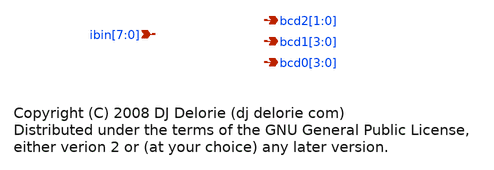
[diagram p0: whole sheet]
** sch_path: xschem_libs_newsym/binto7seg/bcd/schematic/bcd.sch
* Copyright (C) 1998-2024 Stefan Frederik Schippers
* This program is free software; you can redistribute it and/or modify
* it under the terms of the GNU General Public License as published by
* the Free Software Foundation; either version 2 of the License, or
* (at your option) any later version.
* This program is distributed in the hope that it will be useful,
* but WITHOUT ANY WARRANTY; without even the implied warranty of
* MERCHANTABILITY or FITNESS FOR A PARTICULAR PURPOSE.  See the
* GNU General Public License for more details.
* You should have received a copy of the GNU General Public License
* along with this program; if not, write to the Free Software
* C {devices/code} 260 -380 0 0 {name=CODE value="// Copyright (C) 2008 DJ Delorie <dj delorie com>
**.subckt bcd ibin[7],ibin[6],ibin[5],ibin[4],ibin[3],ibin[2],ibin[1],ibin[0] bcd2[1],bcd2[0]
*+ bcd1[3],bcd1[2],bcd1[1],bcd1[0] bcd0[3],bcd0[2],bcd0[1],bcd0[0]
*.ipin ibin[7],ibin[6],ibin[5],ibin[4],ibin[3],ibin[2],ibin[1],ibin[0]
*.opin bcd2[1],bcd2[0]
*.opin bcd1[3],bcd1[2],bcd1[1],bcd1[0]
*.opin bcd0[3],bcd0[2],bcd0[1],bcd0[0]
**** begin user architecture code

// Copyright (C) 2008 DJ Delorie <dj delorie com>
// Distributed under the terms of the GNU General Public License,
// either verion 2 or (at your choice) any later version.

always @ (ibin)
begin

  case (ibin)
    0 : begin bcd2 <= 2'b00; bcd1 <= 4'b0000; bcd0 <= 4'b0000; end
    1 : begin bcd2 <= 2'b00; bcd1 <= 4'b0000; bcd0 <= 4'b0001; end
    2 : begin bcd2 <= 2'b00; bcd1 <= 4'b0000; bcd0 <= 4'b0010; end
    3 : begin bcd2 <= 2'b00; bcd1 <= 4'b0000; bcd0 <= 4'b0011; end
    4 : begin bcd2 <= 2'b00; bcd1 <= 4'b0000; bcd0 <= 4'b0100; end
    5 : begin bcd2 <= 2'b00; bcd1 <= 4'b0000; bcd0 <= 4'b0101; end
    6 : begin bcd2 <= 2'b00; bcd1 <= 4'b0000; bcd0 <= 4'b0110; end
    7 : begin bcd2 <= 2'b00; bcd1 <= 4'b0000; bcd0 <= 4'b0111; end
    8 : begin bcd2 <= 2'b00; bcd1 <= 4'b0000; bcd0 <= 4'b1000; end
    9 : begin bcd2 <= 2'b00; bcd1 <= 4'b0000; bcd0 <= 4'b1001; end
    10 : begin bcd2 <= 2'b00; bcd1 <= 4'b0001; bcd0 <= 4'b0000; end
    11 : begin bcd2 <= 2'b00; bcd1 <= 4'b0001; bcd0 <= 4'b0001; end
    12 : begin bcd2 <= 2'b00; bcd1 <= 4'b0001; bcd0 <= 4'b0010; end
    13 : begin bcd2 <= 2'b00; bcd1 <= 4'b0001; bcd0 <= 4'b0011; end
    14 : begin bcd2 <= 2'b00; bcd1 <= 4'b0001; bcd0 <= 4'b0100; end
    15 : begin bcd2 <= 2'b00; bcd1 <= 4'b0001; bcd0 <= 4'b0101; end
    16 : begin bcd2 <= 2'b00; bcd1 <= 4'b0001; bcd0 <= 4'b0110; end
    17 : begin bcd2 <= 2'b00; bcd1 <= 4'b0001; bcd0 <= 4'b0111; end
    18 : begin bcd2 <= 2'b00; bcd1 <= 4'b0001; bcd0 <= 4'b1000; end
    19 : begin bcd2 <= 2'b00; bcd1 <= 4'b0001; bcd0 <= 4'b1001; end
    20 : begin bcd2 <= 2'b00; bcd1 <= 4'b0010; bcd0 <= 4'b0000; end
    21 : begin bcd2 <= 2'b00; bcd1 <= 4'b0010; bcd0 <= 4'b0001; end
    22 : begin bcd2 <= 2'b00; bcd1 <= 4'b0010; bcd0 <= 4'b0010; end
    23 : begin bcd2 <= 2'b00; bcd1 <= 4'b0010; bcd0 <= 4'b0011; end
    24 : begin bcd2 <= 2'b00; bcd1 <= 4'b0010; bcd0 <= 4'b0100; end
    25 : begin bcd2 <= 2'b00; bcd1 <= 4'b0010; bcd0 <= 4'b0101; end
    26 : begin bcd2 <= 2'b00; bcd1 <= 4'b0010; bcd0 <= 4'b0110; end
    27 : begin bcd2 <= 2'b00; bcd1 <= 4'b0010; bcd0 <= 4'b0111; end
    28 : begin bcd2 <= 2'b00; bcd1 <= 4'b0010; bcd0 <= 4'b1000; end
    29 : begin bcd2 <= 2'b00; bcd1 <= 4'b0010; bcd0 <= 4'b1001; end
    30 : begin bcd2 <= 2'b00; bcd1 <= 4'b0011; bcd0 <= 4'b0000; end
    31 : begin bcd2 <= 2'b00; bcd1 <= 4'b0011; bcd0 <= 4'b0001; end
    32 : begin bcd2 <= 2'b00; bcd1 <= 4'b0011; bcd0 <= 4'b0010; end
    33 : begin bcd2 <= 2'b00; bcd1 <= 4'b0011; bcd0 <= 4'b0011; end
    34 : begin bcd2 <= 2'b00; bcd1 <= 4'b0011; bcd0 <= 4'b0100; end
    35 : begin bcd2 <= 2'b00; bcd1 <= 4'b0011; bcd0 <= 4'b0101; end
    36 : begin bcd2 <= 2'b00; bcd1 <= 4'b0011; bcd0 <= 4'b0110; end
    37 : begin bcd2 <= 2'b00; bcd1 <= 4'b0011; bcd0 <= 4'b0111; end
    38 : begin bcd2 <= 2'b00; bcd1 <= 4'b0011; bcd0 <= 4'b1000; end
    39 : begin bcd2 <= 2'b00; bcd1 <= 4'b0011; bcd0 <= 4'b1001; end
    40 : begin bcd2 <= 2'b00; bcd1 <= 4'b0100; bcd0 <= 4'b0000; end
    41 : begin bcd2 <= 2'b00; bcd1 <= 4'b0100; bcd0 <= 4'b0001; end
    42 : begin bcd2 <= 2'b00; bcd1 <= 4'b0100; bcd0 <= 4'b0010; end
    43 : begin bcd2 <= 2'b00; bcd1 <= 4'b0100; bcd0 <= 4'b0011; end
    44 : begin bcd2 <= 2'b00; bcd1 <= 4'b0100; bcd0 <= 4'b0100; end
    45 : begin bcd2 <= 2'b00; bcd1 <= 4'b0100; bcd0 <= 4'b0101; end
    46 : begin bcd2 <= 2'b00; bcd1 <= 4'b0100; bcd0 <= 4'b0110; end
    47 : begin bcd2 <= 2'b00; bcd1 <= 4'b0100; bcd0 <= 4'b0111; end
    48 : begin bcd2 <= 2'b00; bcd1 <= 4'b0100; bcd0 <= 4'b1000; end
    49 : begin bcd2 <= 2'b00; bcd1 <= 4'b0100; bcd0 <= 4'b1001; end
    50 : begin bcd2 <= 2'b00; bcd1 <= 4'b0101; bcd0 <= 4'b0000; end
    51 : begin bcd2 <= 2'b00; bcd1 <= 4'b0101; bcd0 <= 4'b0001; end
    52 : begin bcd2 <= 2'b00; bcd1 <= 4'b0101; bcd0 <= 4'b0010; end
    53 : begin bcd2 <= 2'b00; bcd1 <= 4'b0101; bcd0 <= 4'b0011; end
    54 : begin bcd2 <= 2'b00; bcd1 <= 4'b0101; bcd0 <= 4'b0100; end
    55 : begin bcd2 <= 2'b00; bcd1 <= 4'b0101; bcd0 <= 4'b0101; end
    56 : begin bcd2 <= 2'b00; bcd1 <= 4'b0101; bcd0 <= 4'b0110; end
    57 : begin bcd2 <= 2'b00; bcd1 <= 4'b0101; bcd0 <= 4'b0111; end
    58 : begin bcd2 <= 2'b00; bcd1 <= 4'b0101; bcd0 <= 4'b1000; end
    59 : begin bcd2 <= 2'b00; bcd1 <= 4'b0101; bcd0 <= 4'b1001; end
    60 : begin bcd2 <= 2'b00; bcd1 <= 4'b0110; bcd0 <= 4'b0000; end
    61 : begin bcd2 <= 2'b00; bcd1 <= 4'b0110; bcd0 <= 4'b0001; end
    62 : begin bcd2 <= 2'b00; bcd1 <= 4'b0110; bcd0 <= 4'b0010; end
    63 : begin bcd2 <= 2'b00; bcd1 <= 4'b0110; bcd0 <= 4'b0011; end
    64 : begin bcd2 <= 2'b00; bcd1 <= 4'b0110; bcd0 <= 4'b0100; end
    65 : begin bcd2 <= 2'b00; bcd1 <= 4'b0110; bcd0 <= 4'b0101; end
    66 : begin bcd2 <= 2'b00; bcd1 <= 4'b0110; bcd0 <= 4'b0110; end
    67 : begin bcd2 <= 2'b00; bcd1 <= 4'b0110; bcd0 <= 4'b0111; end
    68 : begin bcd2 <= 2'b00; bcd1 <= 4'b0110; bcd0 <= 4'b1000; end
    69 : begin bcd2 <= 2'b00; bcd1 <= 4'b0110; bcd0 <= 4'b1001; end
    70 : begin bcd2 <= 2'b00; bcd1 <= 4'b0111; bcd0 <= 4'b0000; end
    71 : begin bcd2 <= 2'b00; bcd1 <= 4'b0111; bcd0 <= 4'b0001; end
    72 : begin bcd2 <= 2'b00; bcd1 <= 4'b0111; bcd0 <= 4'b0010; end
    73 : begin bcd2 <= 2'b00; bcd1 <= 4'b0111; bcd0 <= 4'b0011; end
    74 : begin bcd2 <= 2'b00; bcd1 <= 4'b0111; bcd0 <= 4'b0100; end
    75 : begin bcd2 <= 2'b00; bcd1 <= 4'b0111; bcd0 <= 4'b0101; end
    76 : begin bcd2 <= 2'b00; bcd1 <= 4'b0111; bcd0 <= 4'b0110; end
    77 : begin bcd2 <= 2'b00; bcd1 <= 4'b0111; bcd0 <= 4'b0111; end
    78 : begin bcd2 <= 2'b00; bcd1 <= 4'b0111; bcd0 <= 4'b1000; end
    79 : begin bcd2 <= 2'b00; bcd1 <= 4'b0111; bcd0 <= 4'b1001; end
    80 : begin bcd2 <= 2'b00; bcd1 <= 4'b1000; bcd0 <= 4'b0000; end
    81 : begin bcd2 <= 2'b00; bcd1 <= 4'b1000; bcd0 <= 4'b0001; end
    82 : begin bcd2 <= 2'b00; bcd1 <= 4'b1000; bcd0 <= 4'b0010; end
    83 : begin bcd2 <= 2'b00; bcd1 <= 4'b1000; bcd0 <= 4'b0011; end
    84 : begin bcd2 <= 2'b00; bcd1 <= 4'b1000; bcd0 <= 4'b0100; end
    85 : begin bcd2 <= 2'b00; bcd1 <= 4'b1000; bcd0 <= 4'b0101; end
    86 : begin bcd2 <= 2'b00; bcd1 <= 4'b1000; bcd0 <= 4'b0110; end
    87 : begin bcd2 <= 2'b00; bcd1 <= 4'b1000; bcd0 <= 4'b0111; end
    88 : begin bcd2 <= 2'b00; bcd1 <= 4'b1000; bcd0 <= 4'b1000; end
    89 : begin bcd2 <= 2'b00; bcd1 <= 4'b1000; bcd0 <= 4'b1001; end
    90 : begin bcd2 <= 2'b00; bcd1 <= 4'b1001; bcd0 <= 4'b0000; end
    91 : begin bcd2 <= 2'b00; bcd1 <= 4'b1001; bcd0 <= 4'b0001; end
    92 : begin bcd2 <= 2'b00; bcd1 <= 4'b1001; bcd0 <= 4'b0010; end
    93 : begin bcd2 <= 2'b00; bcd1 <= 4'b1001; bcd0 <= 4'b0011; end
    94 : begin bcd2 <= 2'b00; bcd1 <= 4'b1001; bcd0 <= 4'b0100; end
    95 : begin bcd2 <= 2'b00; bcd1 <= 4'b1001; bcd0 <= 4'b0101; end
    96 : begin bcd2 <= 2'b00; bcd1 <= 4'b1001; bcd0 <= 4'b0110; end
    97 : begin bcd2 <= 2'b00; bcd1 <= 4'b1001; bcd0 <= 4'b0111; end
    98 : begin bcd2 <= 2'b00; bcd1 <= 4'b1001; bcd0 <= 4'b1000; end
    99 : begin bcd2 <= 2'b00; bcd1 <= 4'b1001; bcd0 <= 4'b1001; end
    100 : begin bcd2 <= 2'b01; bcd1 <= 4'b0000; bcd0 <= 4'b0000; end
    101 : begin bcd2 <= 2'b01; bcd1 <= 4'b0000; bcd0 <= 4'b0001; end
    102 : begin bcd2 <= 2'b01; bcd1 <= 4'b0000; bcd0 <= 4'b0010; end
    103 : begin bcd2 <= 2'b01; bcd1 <= 4'b0000; bcd0 <= 4'b0011; end
    104 : begin bcd2 <= 2'b01; bcd1 <= 4'b0000; bcd0 <= 4'b0100; end
    105 : begin bcd2 <= 2'b01; bcd1 <= 4'b0000; bcd0 <= 4'b0101; end
    106 : begin bcd2 <= 2'b01; bcd1 <= 4'b0000; bcd0 <= 4'b0110; end
    107 : begin bcd2 <= 2'b01; bcd1 <= 4'b0000; bcd0 <= 4'b0111; end
    108 : begin bcd2 <= 2'b01; bcd1 <= 4'b0000; bcd0 <= 4'b1000; end
    109 : begin bcd2 <= 2'b01; bcd1 <= 4'b0000; bcd0 <= 4'b1001; end
    110 : begin bcd2 <= 2'b01; bcd1 <= 4'b0001; bcd0 <= 4'b0000; end
    111 : begin bcd2 <= 2'b01; bcd1 <= 4'b0001; bcd0 <= 4'b0001; end
    112 : begin bcd2 <= 2'b01; bcd1 <= 4'b0001; bcd0 <= 4'b0010; end
    113 : begin bcd2 <= 2'b01; bcd1 <= 4'b0001; bcd0 <= 4'b0011; end
    114 : begin bcd2 <= 2'b01; bcd1 <= 4'b0001; bcd0 <= 4'b0100; end
    115 : begin bcd2 <= 2'b01; bcd1 <= 4'b0001; bcd0 <= 4'b0101; end
    116 : begin bcd2 <= 2'b01; bcd1 <= 4'b0001; bcd0 <= 4'b0110; end
    117 : begin bcd2 <= 2'b01; bcd1 <= 4'b0001; bcd0 <= 4'b0111; end
    118 : begin bcd2 <= 2'b01; bcd1 <= 4'b0001; bcd0 <= 4'b1000; end
    119 : begin bcd2 <= 2'b01; bcd1 <= 4'b0001; bcd0 <= 4'b1001; end
    120 : begin bcd2 <= 2'b01; bcd1 <= 4'b0010; bcd0 <= 4'b0000; end
    121 : begin bcd2 <= 2'b01; bcd1 <= 4'b0010; bcd0 <= 4'b0001; end
    122 : begin bcd2 <= 2'b01; bcd1 <= 4'b0010; bcd0 <= 4'b0010; end
    123 : begin bcd2 <= 2'b01; bcd1 <= 4'b0010; bcd0 <= 4'b0011; end
    124 : begin bcd2 <= 2'b01; bcd1 <= 4'b0010; bcd0 <= 4'b0100; end
    125 : begin bcd2 <= 2'b01; bcd1 <= 4'b0010; bcd0 <= 4'b0101; end
    126 : begin bcd2 <= 2'b01; bcd1 <= 4'b0010; bcd0 <= 4'b0110; end
    127 : begin bcd2 <= 2'b01; bcd1 <= 4'b0010; bcd0 <= 4'b0111; end
    128 : begin bcd2 <= 2'b01; bcd1 <= 4'b0010; bcd0 <= 4'b1000; end
    129 : begin bcd2 <= 2'b01; bcd1 <= 4'b0010; bcd0 <= 4'b1001; end
    130 : begin bcd2 <= 2'b01; bcd1 <= 4'b0011; bcd0 <= 4'b0000; end
    131 : begin bcd2 <= 2'b01; bcd1 <= 4'b0011; bcd0 <= 4'b0001; end
    132 : begin bcd2 <= 2'b01; bcd1 <= 4'b0011; bcd0 <= 4'b0010; end
    133 : begin bcd2 <= 2'b01; bcd1 <= 4'b0011; bcd0 <= 4'b0011; end
    134 : begin bcd2 <= 2'b01; bcd1 <= 4'b0011; bcd0 <= 4'b0100; end
    135 : begin bcd2 <= 2'b01; bcd1 <= 4'b0011; bcd0 <= 4'b0101; end
    136 : begin bcd2 <= 2'b01; bcd1 <= 4'b0011; bcd0 <= 4'b0110; end
    137 : begin bcd2 <= 2'b01; bcd1 <= 4'b0011; bcd0 <= 4'b0111; end
    138 : begin bcd2 <= 2'b01; bcd1 <= 4'b0011; bcd0 <= 4'b1000; end
    139 : begin bcd2 <= 2'b01; bcd1 <= 4'b0011; bcd0 <= 4'b1001; end
    140 : begin bcd2 <= 2'b01; bcd1 <= 4'b0100; bcd0 <= 4'b0000; end
    141 : begin bcd2 <= 2'b01; bcd1 <= 4'b0100; bcd0 <= 4'b0001; end
    142 : begin bcd2 <= 2'b01; bcd1 <= 4'b0100; bcd0 <= 4'b0010; end
    143 : begin bcd2 <= 2'b01; bcd1 <= 4'b0100; bcd0 <= 4'b0011; end
    144 : begin bcd2 <= 2'b01; bcd1 <= 4'b0100; bcd0 <= 4'b0100; end
    145 : begin bcd2 <= 2'b01; bcd1 <= 4'b0100; bcd0 <= 4'b0101; end
    146 : begin bcd2 <= 2'b01; bcd1 <= 4'b0100; bcd0 <= 4'b0110; end
    147 : begin bcd2 <= 2'b01; bcd1 <= 4'b0100; bcd0 <= 4'b0111; end
    148 : begin bcd2 <= 2'b01; bcd1 <= 4'b0100; bcd0 <= 4'b1000; end
    149 : begin bcd2 <= 2'b01; bcd1 <= 4'b0100; bcd0 <= 4'b1001; end
    150 : begin bcd2 <= 2'b01; bcd1 <= 4'b0101; bcd0 <= 4'b0000; end
    151 : begin bcd2 <= 2'b01; bcd1 <= 4'b0101; bcd0 <= 4'b0001; end
    152 : begin bcd2 <= 2'b01; bcd1 <= 4'b0101; bcd0 <= 4'b0010; end
    153 : begin bcd2 <= 2'b01; bcd1 <= 4'b0101; bcd0 <= 4'b0011; end
    154 : begin bcd2 <= 2'b01; bcd1 <= 4'b0101; bcd0 <= 4'b0100; end
    155 : begin bcd2 <= 2'b01; bcd1 <= 4'b0101; bcd0 <= 4'b0101; end
    156 : begin bcd2 <= 2'b01; bcd1 <= 4'b0101; bcd0 <= 4'b0110; end
    157 : begin bcd2 <= 2'b01; bcd1 <= 4'b0101; bcd0 <= 4'b0111; end
    158 : begin bcd2 <= 2'b01; bcd1 <= 4'b0101; bcd0 <= 4'b1000; end
    159 : begin bcd2 <= 2'b01; bcd1 <= 4'b0101; bcd0 <= 4'b1001; end
    160 : begin bcd2 <= 2'b01; bcd1 <= 4'b0110; bcd0 <= 4'b0000; end
    161 : begin bcd2 <= 2'b01; bcd1 <= 4'b0110; bcd0 <= 4'b0001; end
    162 : begin bcd2 <= 2'b01; bcd1 <= 4'b0110; bcd0 <= 4'b0010; end
    163 : begin bcd2 <= 2'b01; bcd1 <= 4'b0110; bcd0 <= 4'b0011; end
    164 : begin bcd2 <= 2'b01; bcd1 <= 4'b0110; bcd0 <= 4'b0100; end
    165 : begin bcd2 <= 2'b01; bcd1 <= 4'b0110; bcd0 <= 4'b0101; end
    166 : begin bcd2 <= 2'b01; bcd1 <= 4'b0110; bcd0 <= 4'b0110; end
    167 : begin bcd2 <= 2'b01; bcd1 <= 4'b0110; bcd0 <= 4'b0111; end
    168 : begin bcd2 <= 2'b01; bcd1 <= 4'b0110; bcd0 <= 4'b1000; end
    169 : begin bcd2 <= 2'b01; bcd1 <= 4'b0110; bcd0 <= 4'b1001; end
    170 : begin bcd2 <= 2'b01; bcd1 <= 4'b0111; bcd0 <= 4'b0000; end
    171 : begin bcd2 <= 2'b01; bcd1 <= 4'b0111; bcd0 <= 4'b0001; end
    172 : begin bcd2 <= 2'b01; bcd1 <= 4'b0111; bcd0 <= 4'b0010; end
    173 : begin bcd2 <= 2'b01; bcd1 <= 4'b0111; bcd0 <= 4'b0011; end
    174 : begin bcd2 <= 2'b01; bcd1 <= 4'b0111; bcd0 <= 4'b0100; end
    175 : begin bcd2 <= 2'b01; bcd1 <= 4'b0111; bcd0 <= 4'b0101; end
    176 : begin bcd2 <= 2'b01; bcd1 <= 4'b0111; bcd0 <= 4'b0110; end
    177 : begin bcd2 <= 2'b01; bcd1 <= 4'b0111; bcd0 <= 4'b0111; end
    178 : begin bcd2 <= 2'b01; bcd1 <= 4'b0111; bcd0 <= 4'b1000; end
    179 : begin bcd2 <= 2'b01; bcd1 <= 4'b0111; bcd0 <= 4'b1001; end
    180 : begin bcd2 <= 2'b01; bcd1 <= 4'b1000; bcd0 <= 4'b0000; end
    181 : begin bcd2 <= 2'b01; bcd1 <= 4'b1000; bcd0 <= 4'b0001; end
    182 : begin bcd2 <= 2'b01; bcd1 <= 4'b1000; bcd0 <= 4'b0010; end
    183 : begin bcd2 <= 2'b01; bcd1 <= 4'b1000; bcd0 <= 4'b0011; end
    184 : begin bcd2 <= 2'b01; bcd1 <= 4'b1000; bcd0 <= 4'b0100; end
    185 : begin bcd2 <= 2'b01; bcd1 <= 4'b1000; bcd0 <= 4'b0101; end
    186 : begin bcd2 <= 2'b01; bcd1 <= 4'b1000; bcd0 <= 4'b0110; end
    187 : begin bcd2 <= 2'b01; bcd1 <= 4'b1000; bcd0 <= 4'b0111; end
    188 : begin bcd2 <= 2'b01; bcd1 <= 4'b1000; bcd0 <= 4'b1000; end
    189 : begin bcd2 <= 2'b01; bcd1 <= 4'b1000; bcd0 <= 4'b1001; end
    190 : begin bcd2 <= 2'b01; bcd1 <= 4'b1001; bcd0 <= 4'b0000; end
    191 : begin bcd2 <= 2'b01; bcd1 <= 4'b1001; bcd0 <= 4'b0001; end
    192 : begin bcd2 <= 2'b01; bcd1 <= 4'b1001; bcd0 <= 4'b0010; end
    193 : begin bcd2 <= 2'b01; bcd1 <= 4'b1001; bcd0 <= 4'b0011; end
    194 : begin bcd2 <= 2'b01; bcd1 <= 4'b1001; bcd0 <= 4'b0100; end
    195 : begin bcd2 <= 2'b01; bcd1 <= 4'b1001; bcd0 <= 4'b0101; end
    196 : begin bcd2 <= 2'b01; bcd1 <= 4'b1001; bcd0 <= 4'b0110; end
    197 : begin bcd2 <= 2'b01; bcd1 <= 4'b1001; bcd0 <= 4'b0111; end
    198 : begin bcd2 <= 2'b01; bcd1 <= 4'b1001; bcd0 <= 4'b1000; end
    199 : begin bcd2 <= 2'b01; bcd1 <= 4'b1001; bcd0 <= 4'b1001; end
    200 : begin bcd2 <= 2'b10; bcd1 <= 4'b0000; bcd0 <= 4'b0000; end
    201 : begin bcd2 <= 2'b10; bcd1 <= 4'b0000; bcd0 <= 4'b0001; end
    202 : begin bcd2 <= 2'b10; bcd1 <= 4'b0000; bcd0 <= 4'b0010; end
    203 : begin bcd2 <= 2'b10; bcd1 <= 4'b0000; bcd0 <= 4'b0011; end
    204 : begin bcd2 <= 2'b10; bcd1 <= 4'b0000; bcd0 <= 4'b0100; end
    205 : begin bcd2 <= 2'b10; bcd1 <= 4'b0000; bcd0 <= 4'b0101; end
    206 : begin bcd2 <= 2'b10; bcd1 <= 4'b0000; bcd0 <= 4'b0110; end
    207 : begin bcd2 <= 2'b10; bcd1 <= 4'b0000; bcd0 <= 4'b0111; end
    208 : begin bcd2 <= 2'b10; bcd1 <= 4'b0000; bcd0 <= 4'b1000; end
    209 : begin bcd2 <= 2'b10; bcd1 <= 4'b0000; bcd0 <= 4'b1001; end
    210 : begin bcd2 <= 2'b10; bcd1 <= 4'b0001; bcd0 <= 4'b0000; end
    211 : begin bcd2 <= 2'b10; bcd1 <= 4'b0001; bcd0 <= 4'b0001; end
    212 : begin bcd2 <= 2'b10; bcd1 <= 4'b0001; bcd0 <= 4'b0010; end
    213 : begin bcd2 <= 2'b10; bcd1 <= 4'b0001; bcd0 <= 4'b0011; end
    214 : begin bcd2 <= 2'b10; bcd1 <= 4'b0001; bcd0 <= 4'b0100; end
    215 : begin bcd2 <= 2'b10; bcd1 <= 4'b0001; bcd0 <= 4'b0101; end
    216 : begin bcd2 <= 2'b10; bcd1 <= 4'b0001; bcd0 <= 4'b0110; end
    217 : begin bcd2 <= 2'b10; bcd1 <= 4'b0001; bcd0 <= 4'b0111; end
    218 : begin bcd2 <= 2'b10; bcd1 <= 4'b0001; bcd0 <= 4'b1000; end
    219 : begin bcd2 <= 2'b10; bcd1 <= 4'b0001; bcd0 <= 4'b1001; end
    220 : begin bcd2 <= 2'b10; bcd1 <= 4'b0010; bcd0 <= 4'b0000; end
    221 : begin bcd2 <= 2'b10; bcd1 <= 4'b0010; bcd0 <= 4'b0001; end
    222 : begin bcd2 <= 2'b10; bcd1 <= 4'b0010; bcd0 <= 4'b0010; end
    223 : begin bcd2 <= 2'b10; bcd1 <= 4'b0010; bcd0 <= 4'b0011; end
    224 : begin bcd2 <= 2'b10; bcd1 <= 4'b0010; bcd0 <= 4'b0100; end
    225 : begin bcd2 <= 2'b10; bcd1 <= 4'b0010; bcd0 <= 4'b0101; end
    226 : begin bcd2 <= 2'b10; bcd1 <= 4'b0010; bcd0 <= 4'b0110; end
    227 : begin bcd2 <= 2'b10; bcd1 <= 4'b0010; bcd0 <= 4'b0111; end
    228 : begin bcd2 <= 2'b10; bcd1 <= 4'b0010; bcd0 <= 4'b1000; end
    229 : begin bcd2 <= 2'b10; bcd1 <= 4'b0010; bcd0 <= 4'b1001; end
    230 : begin bcd2 <= 2'b10; bcd1 <= 4'b0011; bcd0 <= 4'b0000; end
    231 : begin bcd2 <= 2'b10; bcd1 <= 4'b0011; bcd0 <= 4'b0001; end
    232 : begin bcd2 <= 2'b10; bcd1 <= 4'b0011; bcd0 <= 4'b0010; end
    233 : begin bcd2 <= 2'b10; bcd1 <= 4'b0011; bcd0 <= 4'b0011; end
    234 : begin bcd2 <= 2'b10; bcd1 <= 4'b0011; bcd0 <= 4'b0100; end
    235 : begin bcd2 <= 2'b10; bcd1 <= 4'b0011; bcd0 <= 4'b0101; end
    236 : begin bcd2 <= 2'b10; bcd1 <= 4'b0011; bcd0 <= 4'b0110; end
    237 : begin bcd2 <= 2'b10; bcd1 <= 4'b0011; bcd0 <= 4'b0111; end
    238 : begin bcd2 <= 2'b10; bcd1 <= 4'b0011; bcd0 <= 4'b1000; end
    239 : begin bcd2 <= 2'b10; bcd1 <= 4'b0011; bcd0 <= 4'b1001; end
    240 : begin bcd2 <= 2'b10; bcd1 <= 4'b0100; bcd0 <= 4'b0000; end
    241 : begin bcd2 <= 2'b10; bcd1 <= 4'b0100; bcd0 <= 4'b0001; end
    242 : begin bcd2 <= 2'b10; bcd1 <= 4'b0100; bcd0 <= 4'b0010; end
    243 : begin bcd2 <= 2'b10; bcd1 <= 4'b0100; bcd0 <= 4'b0011; end
    244 : begin bcd2 <= 2'b10; bcd1 <= 4'b0100; bcd0 <= 4'b0100; end
    245 : begin bcd2 <= 2'b10; bcd1 <= 4'b0100; bcd0 <= 4'b0101; end
    246 : begin bcd2 <= 2'b10; bcd1 <= 4'b0100; bcd0 <= 4'b0110; end
    247 : begin bcd2 <= 2'b10; bcd1 <= 4'b0100; bcd0 <= 4'b0111; end
    248 : begin bcd2 <= 2'b10; bcd1 <= 4'b0100; bcd0 <= 4'b1000; end
    249 : begin bcd2 <= 2'b10; bcd1 <= 4'b0100; bcd0 <= 4'b1001; end
    250 : begin bcd2 <= 2'b10; bcd1 <= 4'b0101; bcd0 <= 4'b0000; end
    251 : begin bcd2 <= 2'b10; bcd1 <= 4'b0101; bcd0 <= 4'b0001; end
    252 : begin bcd2 <= 2'b10; bcd1 <= 4'b0101; bcd0 <= 4'b0010; end
    253 : begin bcd2 <= 2'b10; bcd1 <= 4'b0101; bcd0 <= 4'b0011; end
    254 : begin bcd2 <= 2'b10; bcd1 <= 4'b0101; bcd0 <= 4'b0100; end
    255 : begin bcd2 <= 2'b10; bcd1 <= 4'b0101; bcd0 <= 4'b0101; end
  endcase
end


**** end user architecture code
**.ends
.end
